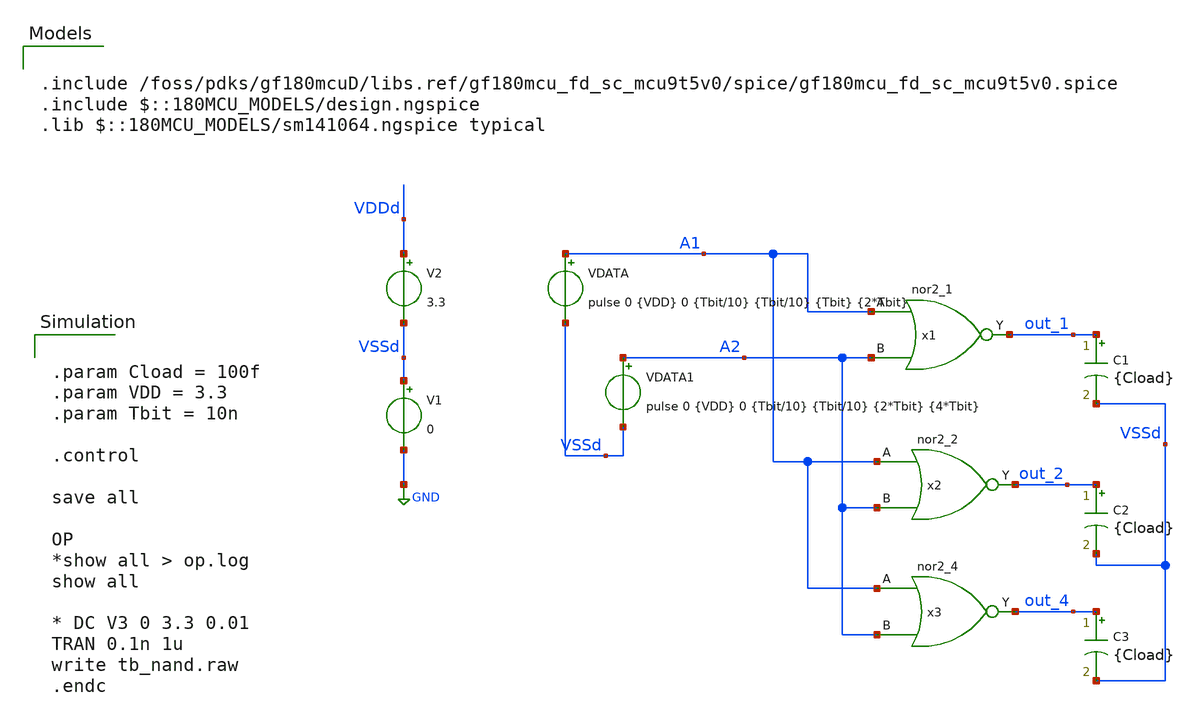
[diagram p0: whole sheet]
** sch_path: designs/libs/tb_digital_cells/tb_nor.sch
**.subckt tb_nor
V1 VSSd GND 0
V2 VDDd VSSd 3.3
x1 A1 A2 VGND VNB VPB VPWR out_1 sky130_fd_sc_hd__nor2_1
VDATA A1 VSSd pulse 0 {VDD} 0 {Tbit/10} {Tbit/10} {Tbit} {2*Tbit}
VDATA1 A2 VSSd pulse 0 {VDD} 0 {Tbit/10} {Tbit/10} {2*Tbit} {4*Tbit}
x2 A1 A2 VSSd VDDd VSSd VDDd out_2 gf180mcu_fd_sc_mcu9t5v0__nor2_2
x3 A1 A2 VSSd VDDd VSSd VDDd out_4 gf180mcu_fd_sc_mcu9t5v0__nor2_4
C1 out_1 VSSd {Cload} m=1
C2 out_2 VSSd {Cload} m=1
C3 out_4 VSSd {Cload} m=1
**** begin user architecture code


.param Cload = 100f
.param VDD = 3.3
.param Tbit = 10n

.control

save all

OP
*show all > op.log
show all

* DC V3 0 3.3 0.01
TRAN 0.1n 1u
write tb_nand.raw
.endc



.include /foss/pdks/gf180mcuD/libs.ref/gf180mcu_fd_sc_mcu9t5v0/spice/gf180mcu_fd_sc_mcu9t5v0.spice
.include $::180MCU_MODELS/design.ngspice
.lib $::180MCU_MODELS/sm141064.ngspice typical

**** end user architecture code
**.ends
.GLOBAL GND
.end
